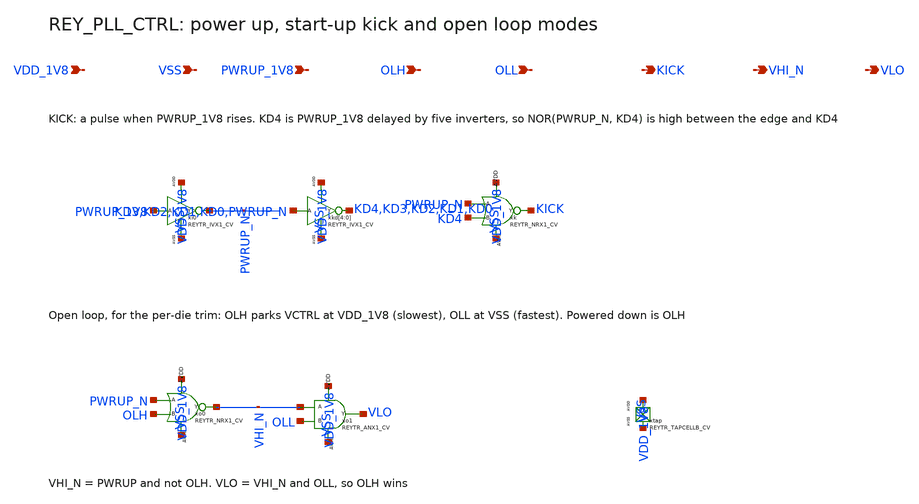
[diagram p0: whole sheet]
** sch_path: design/REY_PLL_SKY130A/REY_PLL_CTRL.sch
**.subckt REY_PLL_CTRL VDD_1V8 VSS PWRUP_1V8 OLH OLL KICK VHI_N VLO
*.ipin VDD_1V8
*.ipin VSS
*.ipin PWRUP_1V8
*.ipin OLH
*.ipin OLL
*.opin KICK
*.opin VHI_N
*.opin VLO
xi0 PWRUP_1V8 PWRUP_N VDD_1V8 VSS REYTR_IVX1_CV
xkd[4] KD3 KD4 VDD_1V8 VSS REYTR_IVX1_CV
xkd[3] KD2 KD3 VDD_1V8 VSS REYTR_IVX1_CV
xkd[2] KD1 KD2 VDD_1V8 VSS REYTR_IVX1_CV
xkd[1] KD0 KD1 VDD_1V8 VSS REYTR_IVX1_CV
xkd[0] PWRUP_N KD0 VDD_1V8 VSS REYTR_IVX1_CV
xk PWRUP_N KD4 KICK VDD_1V8 VSS REYTR_NRX1_CV
xo0 PWRUP_N OLH VHI_N VDD_1V8 VSS REYTR_NRX1_CV
xo1 VHI_N OLL VLO VDD_1V8 VSS REYTR_ANX1_CV xoffset=0 yoffset=0 angle=0 M=1
xtap VDD_1V8 VSS REYTR_TAPCELLB_CV xoffset=0 yoffset=0 angle=0
**.ends
.end
